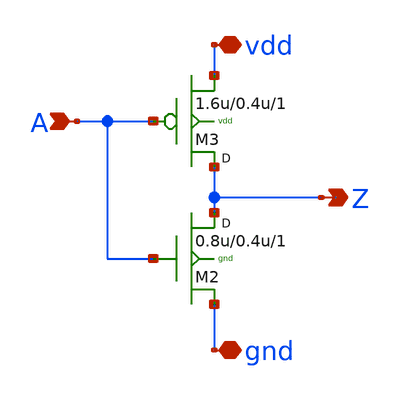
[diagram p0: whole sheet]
** sch_path: sram_4_16_scn4m/pinv_12.sch
**.subckt pinv_12 A Z vdd gnd
*.ipin A
*.opin Z
*.iopin vdd
*.iopin gnd
M2 Z A gnd gnd n w=0.8u l=0.4u m=1
M3 Z A vdd vdd p w=1.6u l=0.4u m=1
**.ends
.end
